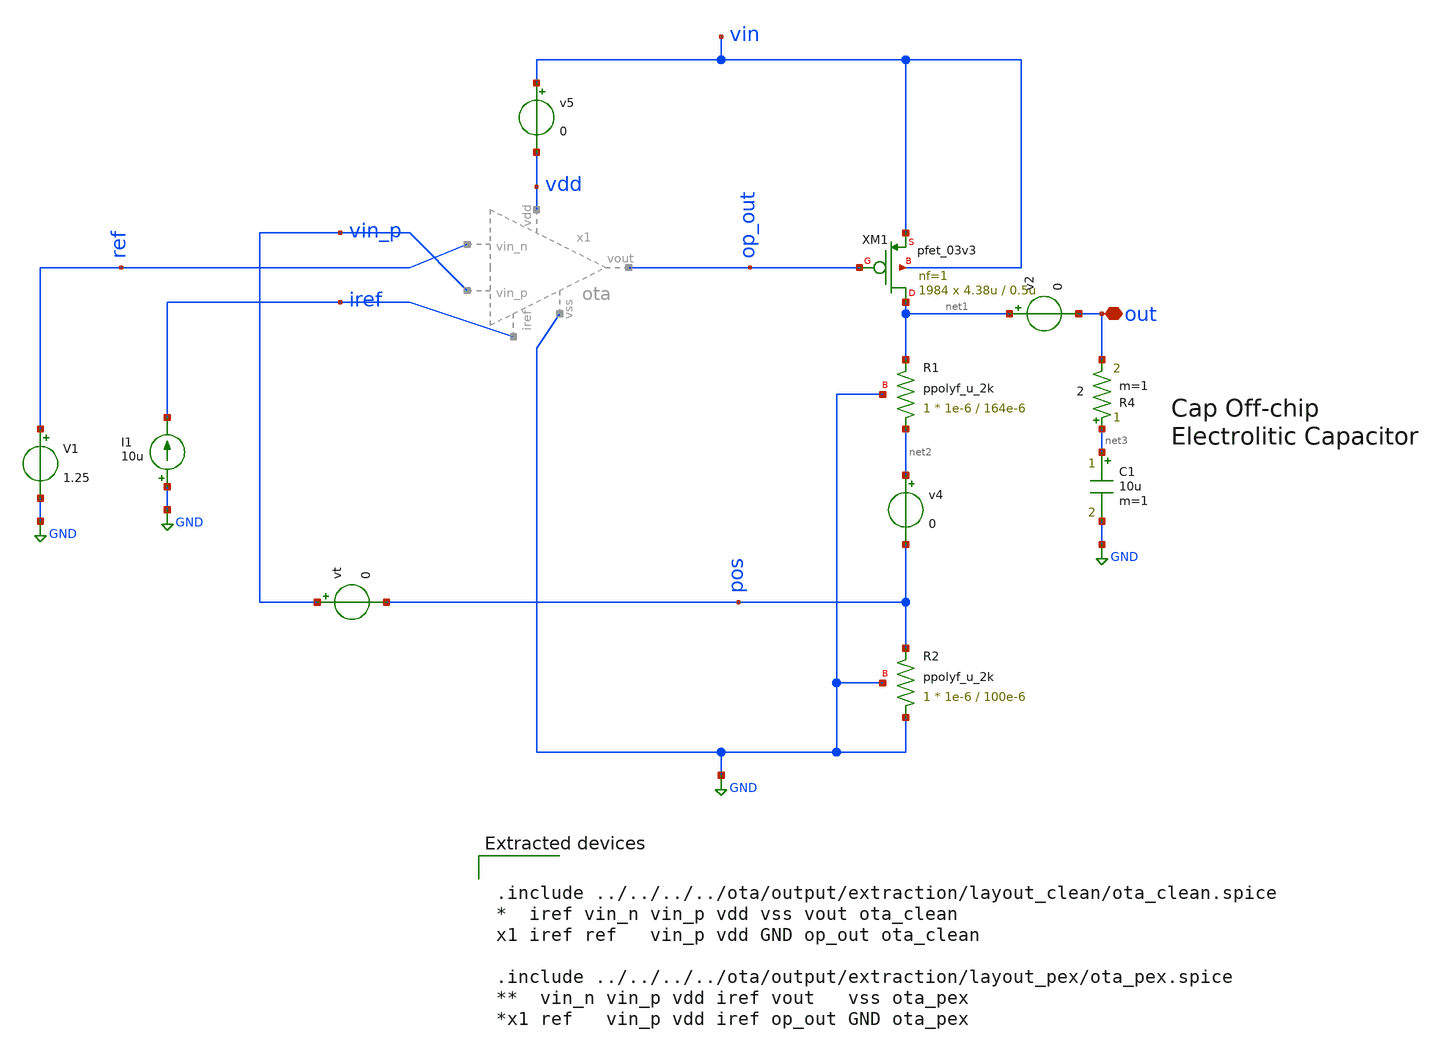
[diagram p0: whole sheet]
** sch_path: LDO/xschem/ldo/test/line_regulation.sch

.include $env(PDK_ROOT)/$env(PDK)/libs.tech/ngspice/design.ngspice
.lib $env(PDK_ROOT)/$env(PDK)/libs.tech/ngspice/sm141064.ngspice typical
.lib $env(PDK_ROOT)/$env(PDK)/libs.tech/ngspice/sm141064.ngspice res_typical

.lib $env(PDK_ROOT)/$env(PDK)/libs.tech/ngspice/sm141064.ngspice cap_mim
.lib $env(PDK_ROOT)/$env(PDK)/libs.tech/ngspice/sm141064.ngspice mimcap_typical


**.subckt line_regulation out
*.iopin out
I1 GND iref 10u
V1 ref GND 1.25
XM1 net1 op_out vin vin pfet_03v3 L=0.5u W=4.38u nf=1 ad='int((nf+1)/2) * W/nf * 0.18u' as='int((nf+2)/2) * W/nf * 0.18u'
+ pd='2*int((nf+1)/2) * (W/nf + 0.18u)' ps='2*int((nf+2)/2) * (W/nf + 0.18u)' nrd='0.18u / W' nrs='0.18u / W'
+ sa=0 sb=0 sd=0 m=1984
XR1 net2 net1 GND ppolyf_u_2k r_width=1e-6 r_length=164e-6 m=1
XR2 GND pos GND ppolyf_u_2k r_width=1e-6 r_length=100e-6 m=1
v4 net2 pos 0
vt vin_p pos 0
v2 net1 out 0
v5 vin vdd 0
C1 net3 GND 10u m=1
R4 net3 out 2 m=1
**** begin user architecture code


.param R=33
R10 out 0 {R}
IL out 0 PWL(0 0.1m 10u 0.1m 20u 10m 30u 10m)

.param iref = 10u
.param vdd  = 5
.param vss  = 0.0
.param vcm  = 1.25
.param vac  = 60m
.param w857 = 5u
.param l857 = 1u
.param m857 = 1
.param wpar = 10u
.param lpar = 1u
.param mpar = 1
.param w34  = 10u
.param l34  = 1u
.param m34  = 1
.param w6   = 100u
.param l6   = 1u
.param m6   = 1

.param m5   = 1
.param m7   = 5


Vs vin 0 5

.nodeset v(out)=0
.nodeset v(x1.pos)=0

*supply_sweep
.control
reseet
alter IL 0
dc Vs 6 0 -0.1
plot v(vin) v(out)
meas DC vldo_sup_4_6 FIND v(out) AT=4.6
meas DC vldo_nom FIND v(out) AT=5
meas DC vldo_sup_5_4 FIND v(out) AT=5.4
let line_reg = abs((vldo_sup_5_4-vldo_sup_4_6)/0.8)
print line_reg
meas DC vin WHEN v(out)=3.2982
let dropout = vin-3.2982
print dropout
.endc




.include ../../../../ota/output/extraction/layout_clean/ota_clean.spice
*  iref vin_n vin_p vdd vss vout ota_clean
x1 iref ref   vin_p vdd GND op_out ota_clean

.include ../../../../ota/output/extraction/layout_pex/ota_pex.spice
**  vin_n vin_p vdd iref vout   vss ota_pex
*x1 ref   vin_p vdd iref op_out GND ota_pex


**** end user architecture code
**.ends
.GLOBAL GND
.end
